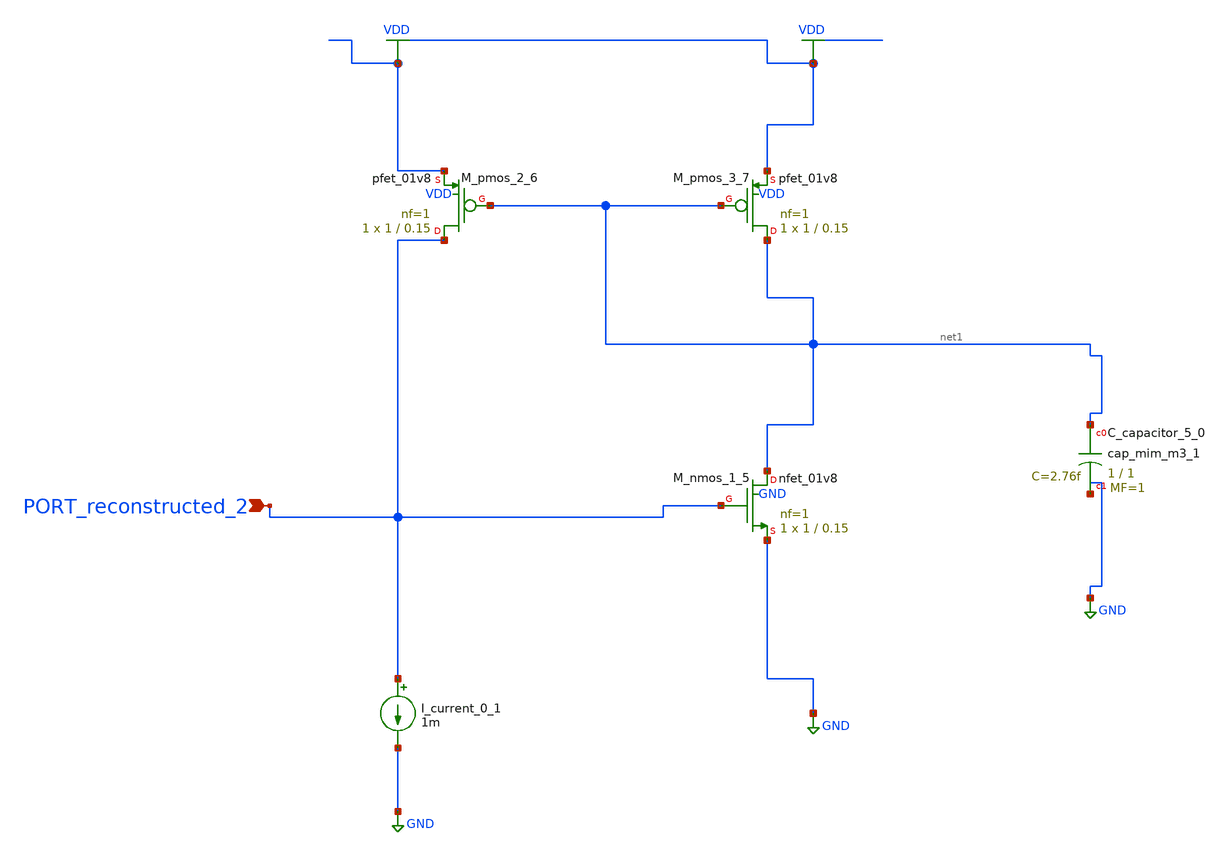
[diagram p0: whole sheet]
** sch_path: schematics/AMSNet/621.sch
**.subckt 621 PORT_reconstructed_2
*.ipin PORT_reconstructed_2
XC_capacitor_5_0 net1 GND sky130_fd_pr__cap_mim_m3_1 W=1 L=1 MF=1 m=1
I_current_0_1 PORT_reconstructed_2 GND 1m
XM_nmos_1_5 net1 PORT_reconstructed_2 GND GND sky130_fd_pr__nfet_01v8 L=0.15 W=1 nf=1 ad='int((1 + 1)/2) * 1 / 1 * 0.29'
+ as='int((1 + 2)/2) * 1 / 1 * 0.29' pd='2*int((1 + 1)/2) * (1 / 1 + 0.29)' ps='2*int((1 + 2)/2) * (1 / 1 + 0.29)'
+ nrd='0.29 / 1 ' nrs='0.29 / 1 ' sa=0 sb=0 sd=0 mult=1 m=1
XM_pmos_2_6 PORT_reconstructed_2 net1 VDD VDD sky130_fd_pr__pfet_01v8 L=0.15 W=1 nf=1 ad='int((1 + 1)/2) * 1 / 1 * 0.29'
+ as='int((1 + 2)/2) * 1 / 1 * 0.29' pd='2*int((1 + 1)/2) * (1 / 1 + 0.29)' ps='2*int((1 + 2)/2) * (1 / 1 + 0.29)'
+ nrd='0.29 / 1 ' nrs='0.29 / 1 ' sa=0 sb=0 sd=0 mult=1 m=1
XM_pmos_3_7 net1 net1 VDD VDD sky130_fd_pr__pfet_01v8 L=0.15 W=1 nf=1 ad='int((1 + 1)/2) * 1 / 1 * 0.29'
+ as='int((1 + 2)/2) * 1 / 1 * 0.29' pd='2*int((1 + 1)/2) * (1 / 1 + 0.29)' ps='2*int((1 + 2)/2) * (1 / 1 + 0.29)'
+ nrd='0.29 / 1 ' nrs='0.29 / 1 ' sa=0 sb=0 sd=0 mult=1 m=1
**.ends
.GLOBAL GND
.GLOBAL VDD
.end
